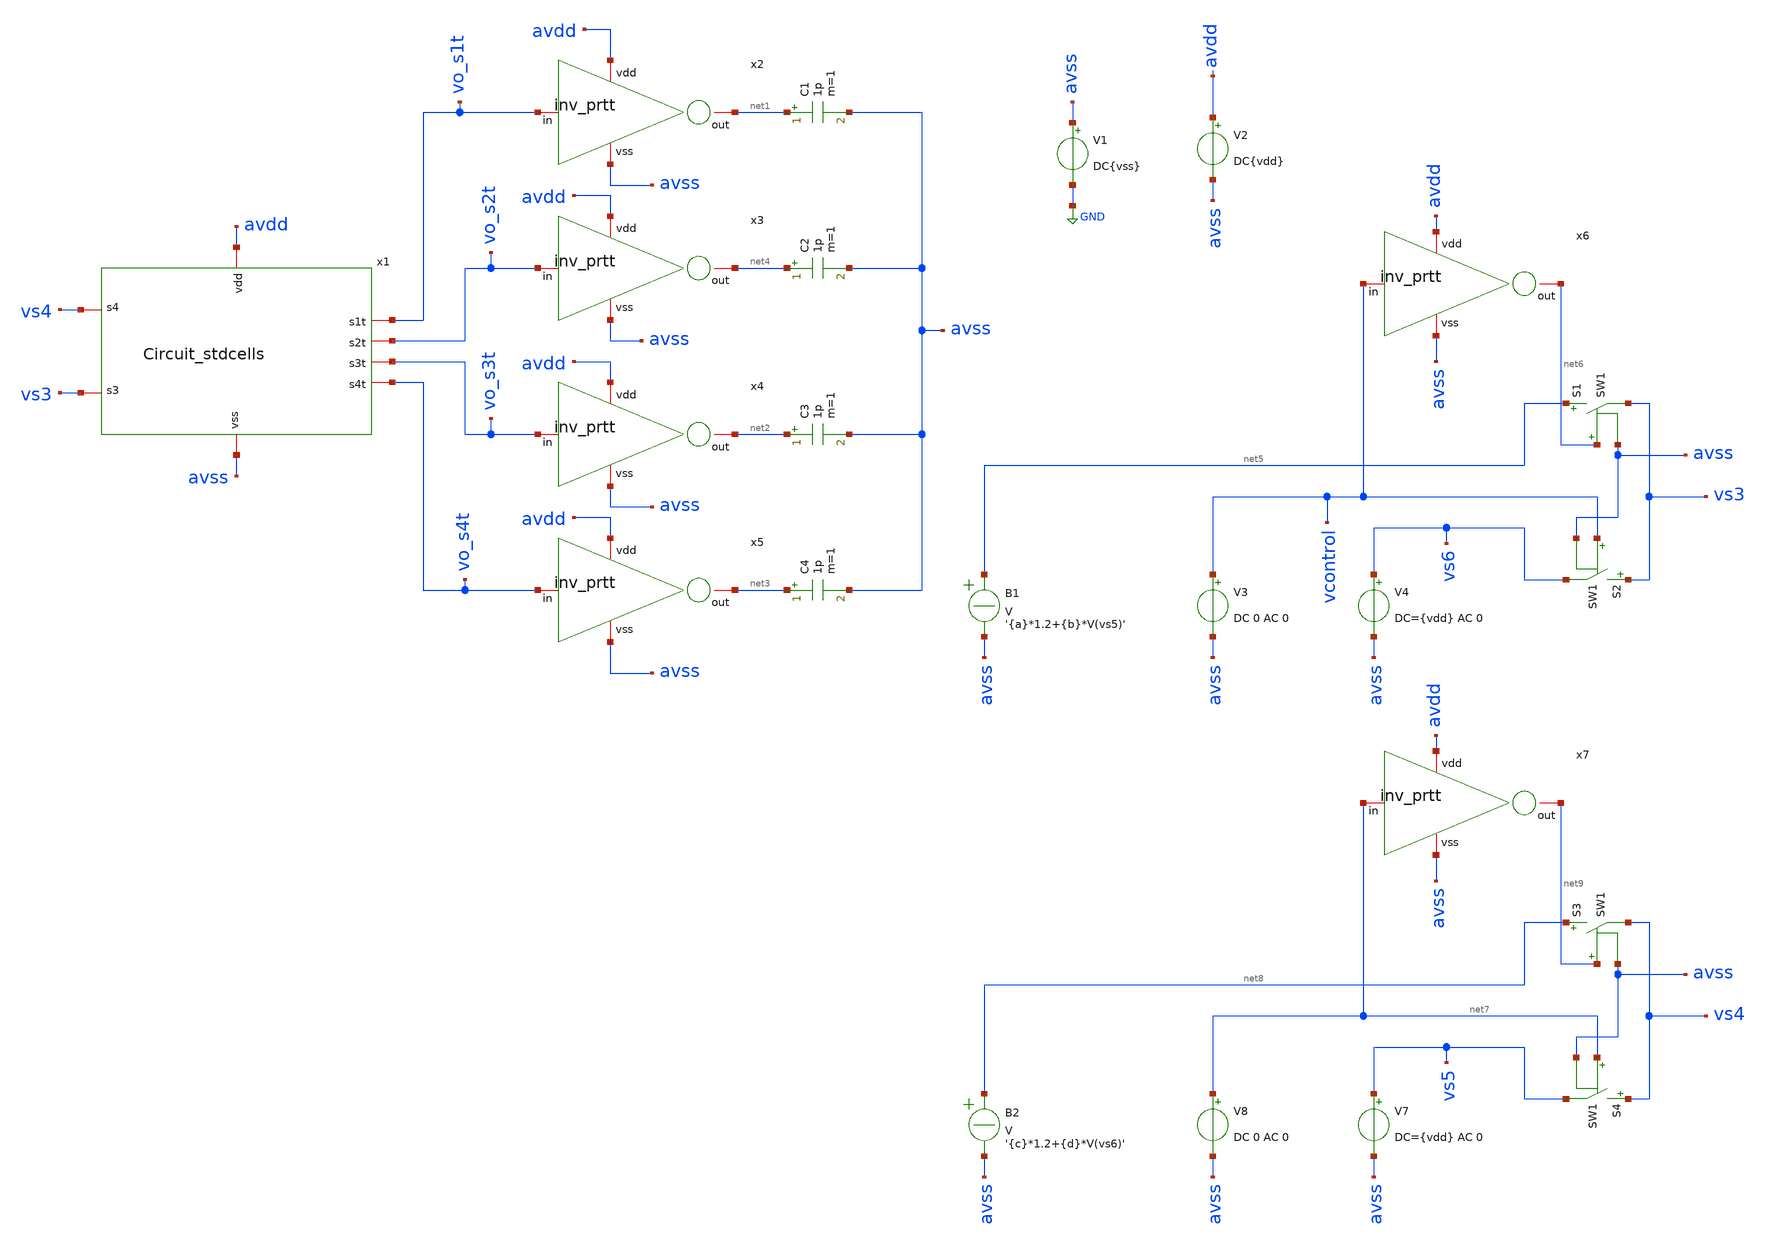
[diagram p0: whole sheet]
** sch_path: PhaseInterpolator/BinarytoThermo/tb_Circuit_stdcells_bsources.sch
**.subckt tb_Circuit_stdcells_bsources
C1 net1 avss 1p m=1
C2 net4 avss 1p m=1
C3 net2 avss 1p m=1
C4 net3 avss 1p m=1
V1 avss GND DC{vss}
V2 avdd avss DC{vdd}
V4 vs6 avss DC={vdd} AC 0
x1 vs4 vs3 vo_s1t vo_s2t vo_s3t avdd vo_s4t avss Circuit_stdcells
x2 avdd vo_s1t net1 avss inv_prtt
x3 avdd vo_s2t net4 avss inv_prtt
x4 avdd vo_s3t net2 avss inv_prtt
x5 avdd vo_s4t net3 avss inv_prtt
B1 net5 avss V = '{a}*1.2+{b}*V(vs5)'
V3 vcontrol avss DC 0 AC 0
S1 net5 vs3 net6 avss SW1
S2 vs3 vs6 vcontrol avss SW1
x6 avdd vcontrol net6 avss inv_prtt
V7 vs5 avss DC={vdd} AC 0
B2 net8 avss V = '{c}*1.2+{d}*V(vs6)'
V8 net7 avss DC 0 AC 0
S3 net8 vs4 net9 avss SW1
S4 vs4 vs5 net7 avss SW1
x7 avdd net7 net9 avss inv_prtt
**** begin user architecture code



* Circuit Parameters
.param vdd = 1.2
.param vss = 0.0
.param a=0
.param b=0
.param c=0
.param d=0
.param Tclk = 500n
.options TEMP = 65.0

* Include Models
.lib /foss/pdks/ihp-sg13g2/libs.tech/ngspice/models/cornerMOSlv.lib mos_tt
.lib /foss/pdks/ihp-sg13g2/libs.tech/ngspice/models/cornerMOShv.lib mos_tt
.lib /foss/pdks/ihp-sg13g2/libs.tech/ngspice/models/cornerHBT.lib hbt_typ
.lib /foss/pdks/ihp-sg13g2/libs.tech/ngspice/models/cornerRES.lib res_typ


* OP Parameters & Singals to save
.save all

*Simulations
.control
	* Desde (s3,s4)=00 a 01
	alter V3=1.2
	alter V8=1.2
	alter V4=0
	dc V7 0 1.2 0.001
	setplot dc1
	plot vs3 vs4 vo_s3t ylabel vout xlabel vin
	set filetype = ascii
	write dc00to01.raw V(vo_s3t) V(vs3) V(vs4)
	* Desde (s3,s4)=00 a 10
	reset
	alter V3=1.2
	alter V8=1.2
	alter V7=0
	dc V4 0 1.2 0.001
	setplot dc2
	plot vs3 vs4 vo_s2t vo_s3t ylabel vout xlabel vin
	set filetype = ascii
	write dc00to10.raw V(vo_s2t) V(vo_s3t) V(vs3) V(vs4)
	* Desde (s3,s4)=00 a 11
	alterparam b = 1
	reset
	alter V3=0
	alter V8=1.2
	dc V7 0 1.2 0.001
	setplot dc3
	plot vs3 vs4 vo_s1t vo_s2t vo_s3t ylabel vout xlabel vin
	set filetype = ascii
	write dc00to11.raw V(vo_s1t) V(vo_s2t) V(vo_s3t) V(vs3) V(vs4)
	* Desde (s3,s4)=01 a 10
	alterparam c=1
	alterparam d=-1
	reset
	alter V3=1.2
	alter V8=0
	dc V4 0 1.2 0.001
	setplot dc4
	plot vs3 vs4 vo_s2t ylabel vout xlabel vin
	set filetype = ascii
	write dc01to10.raw V(vo_s2t) V(vs3) V(vs4)
	* Desde (s3,s4)=01 a 11
	reset
	alter V3=1.2
	alter V8=1.2
	alter V7=1.2
	dc V4 0 1.2 0.001
	setplot dc5
	plot vs3 vs4 vo_s1t vo_s2t ylabel vout xlabel vin
	set filetype = ascii
	write dc01to11.raw V(vo_s1t) V(vo_s2t) V(vs3) V(vs4)
	* Desde (s3,s4)=10 a 11
	reset
	alter V3=1.2
	alter V8=1.2
	alter V4=1.2
	dc V7 0 1.2 0.001
	setplot dc6
	plot vs3 vs4 vo_s1t ylabel vout xlabel vin ylimit 0 1.2
	set filetype = ascii
	write dc10to11.raw V(vo_s1t) V(vs3) V(vs4)
.endc
.end

**** end user architecture code
**.ends
.GLOBAL GND
**** begin user architecture code
.MODEL SW1 SW   VT=0.9 VH=0.01  RON=0.01 ROFF=10G
**** end user architecture code
.end
